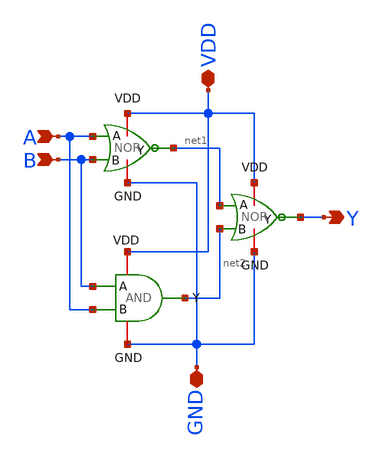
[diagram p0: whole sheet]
** sch_path: FinalProj/XOR.sch
**.subckt XOR A B VDD GND Y
*.ipin A
*.ipin B
*.iopin VDD
*.iopin GND
*.opin Y
x1 VDD B net1 A GND NOR
x2 VDD net2 Y net1 GND NOR
x3 VDD B net2 A GND AND
**.ends

* expanding   symbol:  workspace/FinalProj/NOR.sym # of pins=5
** sym_path: FinalProj/NOR.sym
** sch_path: FinalProj/NOR.sch
.subckt NOR VDD B Y A GND
*.ipin B
*.ipin A
*.iopin GND
*.iopin VDD
*.opin Y
XM1 net1 A VDD VDD sky130_fd_pr__pfet_01v8 L=0.5 W=2 nf=1 ad='int((nf+1)/2) * W/nf * 0.29' as='int((nf+2)/2) * W/nf * 0.29'
+ pd='2*int((nf+1)/2) * (W/nf + 0.29)' ps='2*int((nf+2)/2) * (W/nf + 0.29)' nrd='0.29 / W' nrs='0.29 / W'
+ sa=0 sb=0 sd=0 mult=1 m=1
XM2 Y B net1 VDD sky130_fd_pr__pfet_01v8 L=0.5 W=2 nf=1 ad='int((nf+1)/2) * W/nf * 0.29' as='int((nf+2)/2) * W/nf * 0.29'
+ pd='2*int((nf+1)/2) * (W/nf + 0.29)' ps='2*int((nf+2)/2) * (W/nf + 0.29)' nrd='0.29 / W' nrs='0.29 / W'
+ sa=0 sb=0 sd=0 mult=1 m=1
XM3 Y A GND GND sky130_fd_pr__nfet_01v8 L=0.5 W=0.5 nf=1 ad='int((nf+1)/2) * W/nf * 0.29' as='int((nf+2)/2) * W/nf * 0.29'
+ pd='2*int((nf+1)/2) * (W/nf + 0.29)' ps='2*int((nf+2)/2) * (W/nf + 0.29)' nrd='0.29 / W' nrs='0.29 / W'
+ sa=0 sb=0 sd=0 mult=1 m=1
XM4 Y B GND GND sky130_fd_pr__nfet_01v8 L=0.5 W=0.5 nf=1 ad='int((nf+1)/2) * W/nf * 0.29' as='int((nf+2)/2) * W/nf * 0.29'
+ pd='2*int((nf+1)/2) * (W/nf + 0.29)' ps='2*int((nf+2)/2) * (W/nf + 0.29)' nrd='0.29 / W' nrs='0.29 / W'
+ sa=0 sb=0 sd=0 mult=1 m=1
.ends


* expanding   symbol:  workspace/FinalProj/AND.sym # of pins=5
** sym_path: FinalProj/AND.sym
** sch_path: FinalProj/AND.sch
.subckt AND VDD A Y B GND
*.ipin A
*.ipin B
*.iopin VDD
*.iopin GND
*.opin Y
x1 VDD net1 B A GND NAND
x2 VDD net1 Y GND Inv
.ends


* expanding   symbol:  workspace/FinalProj/NAND.sym # of pins=5
** sym_path: FinalProj/NAND.sym
** sch_path: FinalProj/NAND.sch
.subckt NAND VDD Y B A GND
*.ipin A
*.ipin B
*.iopin VDD
*.iopin GND
*.opin Y
XM1 Y B VDD VDD sky130_fd_pr__pfet_01v8 L=0.5 W=2 nf=1 ad='int((nf+1)/2) * W/nf * 0.29' as='int((nf+2)/2) * W/nf * 0.29'
+ pd='2*int((nf+1)/2) * (W/nf + 0.29)' ps='2*int((nf+2)/2) * (W/nf + 0.29)' nrd='0.29 / W' nrs='0.29 / W'
+ sa=0 sb=0 sd=0 mult=1 m=1
XM2 Y A VDD VDD sky130_fd_pr__pfet_01v8 L=0.5 W=2 nf=1 ad='int((nf+1)/2) * W/nf * 0.29' as='int((nf+2)/2) * W/nf * 0.29'
+ pd='2*int((nf+1)/2) * (W/nf + 0.29)' ps='2*int((nf+2)/2) * (W/nf + 0.29)' nrd='0.29 / W' nrs='0.29 / W'
+ sa=0 sb=0 sd=0 mult=1 m=1
XM3 Y B net1 GND sky130_fd_pr__nfet_01v8 L=0.5 W=2 nf=1 ad='int((nf+1)/2) * W/nf * 0.29' as='int((nf+2)/2) * W/nf * 0.29'
+ pd='2*int((nf+1)/2) * (W/nf + 0.29)' ps='2*int((nf+2)/2) * (W/nf + 0.29)' nrd='0.29 / W' nrs='0.29 / W'
+ sa=0 sb=0 sd=0 mult=1 m=1
XM4 net1 A GND GND sky130_fd_pr__nfet_01v8 L=0.5 W=2 nf=1 ad='int((nf+1)/2) * W/nf * 0.29' as='int((nf+2)/2) * W/nf * 0.29'
+ pd='2*int((nf+1)/2) * (W/nf + 0.29)' ps='2*int((nf+2)/2) * (W/nf + 0.29)' nrd='0.29 / W' nrs='0.29 / W'
+ sa=0 sb=0 sd=0 mult=1 m=1
.ends


* expanding   symbol:  workspace/FinalProj/Inv.sym # of pins=4
** sym_path: FinalProj/Inv.sym
** sch_path: FinalProj/Inv.sch
.subckt Inv VDD A Y GND
*.ipin A
*.iopin GND
*.iopin VDD
*.opin Y
XM1 Y A VDD VDD sky130_fd_pr__pfet_01v8 L=0.5 W=1 nf=1 ad='int((nf+1)/2) * W/nf * 0.29' as='int((nf+2)/2) * W/nf * 0.29'
+ pd='2*int((nf+1)/2) * (W/nf + 0.29)' ps='2*int((nf+2)/2) * (W/nf + 0.29)' nrd='0.29 / W' nrs='0.29 / W'
+ sa=0 sb=0 sd=0 mult=1 m=1
XM2 Y A GND GND sky130_fd_pr__nfet_01v8 L=0.5 W=0.5 nf=1 ad='int((nf+1)/2) * W/nf * 0.29' as='int((nf+2)/2) * W/nf * 0.29'
+ pd='2*int((nf+1)/2) * (W/nf + 0.29)' ps='2*int((nf+2)/2) * (W/nf + 0.29)' nrd='0.29 / W' nrs='0.29 / W'
+ sa=0 sb=0 sd=0 mult=1 m=1
.ends

.end
